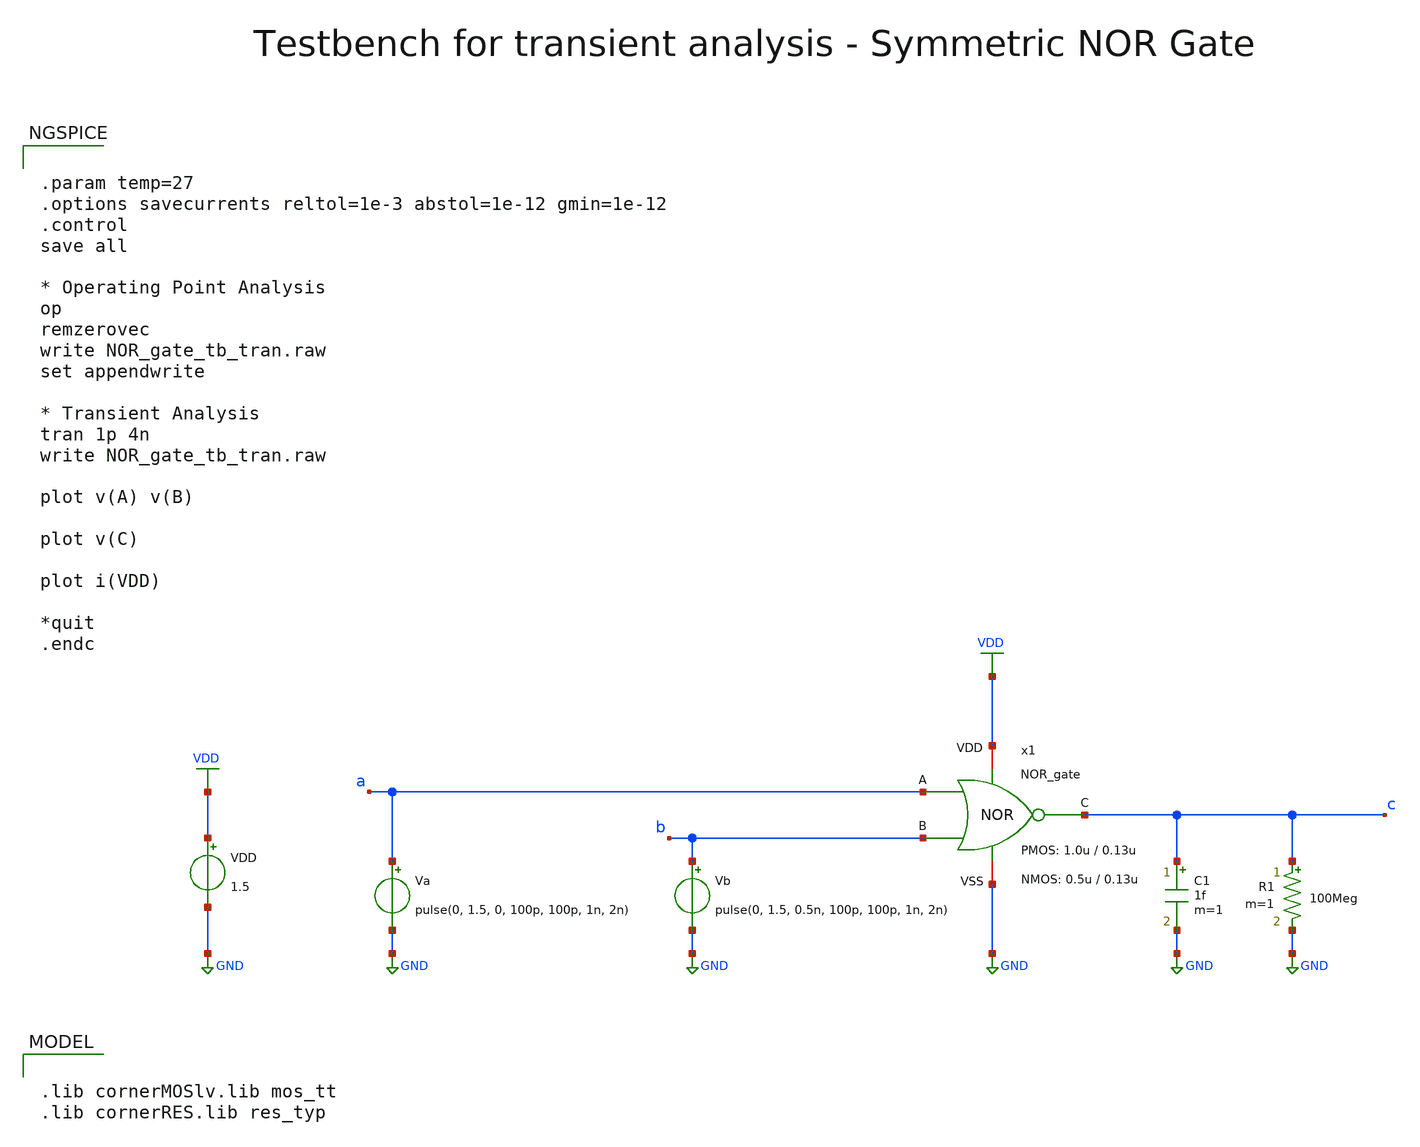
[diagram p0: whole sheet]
** sch_path: SG13G2_ATBS-ADC-main/xschem/comparator/NOR_gate/testbenches/NOR_gate_tb_tran.sch
**.subckt NOR_gate_tb_tran
VDD VDD GND 1.5
Vb b GND pulse(0, 1.5, 0.5n, 100p, 100p, 1n, 2n)
Va a GND pulse(0, 1.5, 0, 100p, 100p, 1n, 2n)
C1 c GND 1f m=1
R1 c GND 100Meg m=1
x1 VDD c a b GND NOR_gate W_P=1.0u L_P=0.13u W_N=0.5u L_N=0.13u
**** begin user architecture code

.lib cornerMOSlv.lib mos_tt
.lib cornerRES.lib res_typ



.param temp=27
.options savecurrents reltol=1e-3 abstol=1e-12 gmin=1e-12
.control
save all

* Operating Point Analysis
op
remzerovec
write NOR_gate_tb_tran.raw
set appendwrite

* Transient Analysis
tran 1p 4n
write NOR_gate_tb_tran.raw

plot v(A) v(B)

plot v(C)

plot i(VDD)

*quit
.endc

**** end user architecture code
**.ends

* expanding   symbol:  comparator/NOR_gate/NOR_gate.sym # of pins=5
** sym_path: SG13G2_ATBS-ADC-main/xschem/comparator/NOR_gate/NOR_gate.sym
** sch_path: SG13G2_ATBS-ADC-main/xschem/comparator/NOR_gate/NOR_gate.sch
.subckt NOR_gate VDD C A B VSS  W_P=1.0u L_P=0.13u W_N=0.5u L_N=0.13u
*.iopin VDD
*.opin C
*.iopin VSS
*.ipin A
*.ipin B
XM1 C A VSS VSS sg13_lv_nmos w=W_N l=L_N ng=1 m=1 mm_ok=1
XM2 C B VSS VSS sg13_lv_nmos w=W_N l=L_N ng=1 m=1 mm_ok=1
XM3 C B net1 VDD sg13_lv_pmos w=W_P l=L_P ng=1 m=1 mm_ok=1
XM4 net1 A VDD VDD sg13_lv_pmos w=W_P l=L_P ng=1 m=1 mm_ok=1
XM5 C A net2 VDD sg13_lv_pmos w=W_P l=L_P ng=1 m=1 mm_ok=1
XM6 net2 B VDD VDD sg13_lv_pmos w=W_P l=L_P ng=1 m=1 mm_ok=1
.ends

.GLOBAL GND
.GLOBAL VDD
.end
